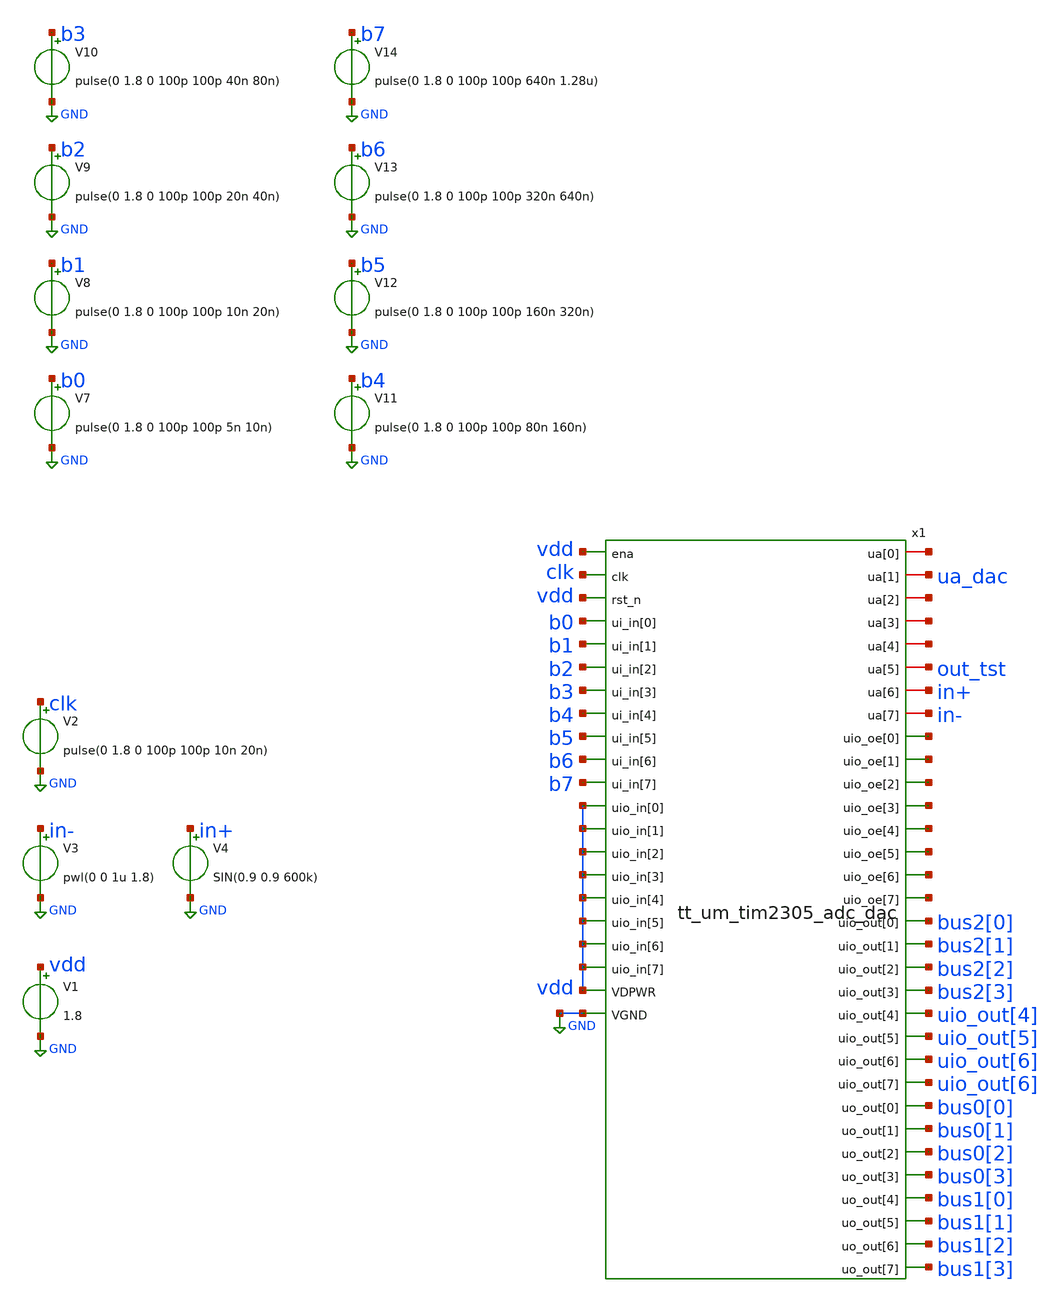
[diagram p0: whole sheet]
** sch_path: xschem/top_tb.sch
**.subckt top_tb
V1 vdd GND 1.8
V3 in- GND pwl(0 0 1u 1.8)
V2 clk GND pulse(0 1.8 0 100p 100p 10n 20n)
x1 net1 ua_dac net2 net3 net4 out_tst in+ vdd in- clk vdd net5 b0 net6 b1 net7 net8 b2 b3 net9 b4
+ net10 b5 net11 net12 b6 b7 bus2[0] vdd bus2[1] vdd bus2[2] vdd bus2[3] uio_out[4] vdd uio_out[5] vdd
+ uio_out[6] vdd vdd uio_out[6] vdd bus0[0] vdd bus0[1] GND bus0[2] bus0[3] bus1[0] bus1[1] bus1[2] bus1[3]
+ tt_um_tim2305_adc_dac
V4 in+ GND SIN(0.9 0.9 600k)
V7 b0 GND pulse(0 1.8 0 100p 100p 5n 10n)
V8 b1 GND pulse(0 1.8 0 100p 100p 10n 20n)
V9 b2 GND pulse(0 1.8 0 100p 100p 20n 40n)
V10 b3 GND pulse(0 1.8 0 100p 100p 40n 80n)
V11 b4 GND pulse(0 1.8 0 100p 100p 80n 160n)
V12 b5 GND pulse(0 1.8 0 100p 100p 160n 320n)
V13 b6 GND pulse(0 1.8 0 100p 100p 320n 640n)
V14 b7 GND pulse(0 1.8 0 100p 100p 640n 1.28u)
**** begin user architecture code


.tran 100p 1u
.save all
.lib /home/ttuser/pdk/sky130A/libs.tech/ngspice/sky130.lib.spice tt
.include /home/ttuser/Documents/github_project/adc_dac2/tt_um_tim2305_adc_dac.spice


**** end user architecture code
**.ends
.GLOBAL GND
.end
